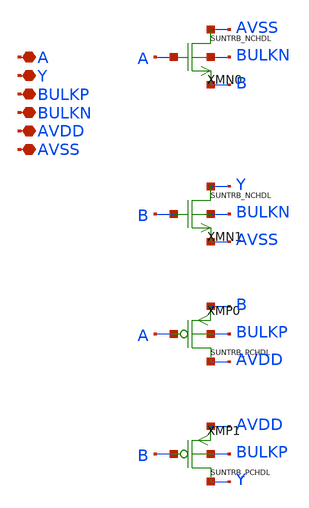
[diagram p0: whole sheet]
** sch_path: design/SUN_TRB_SKY130NM/SUNTRB_BFX1_CV.sch
**.subckt SUNTRB_BFX1_CV A Y BULKP BULKN AVDD AVSS
*.iopin A
*.iopin Y
*.iopin BULKP
*.iopin BULKN
*.iopin AVDD
*.iopin AVSS
XMN0 AVSS A B BULKN SUNTRB_NCHDL xoffset=0 yoffset=0 angle=0
XMN1 Y B AVSS BULKN SUNTRB_NCHDL xoffset=0 yoffset=0 angle=0
XMP0 AVDD A B BULKP SUNTRB_PCHDL xoffset=0 yoffset=0 angle=0 M=1
XMP1 Y B AVDD BULKP SUNTRB_PCHDL xoffset=0 yoffset=0 angle=0 M=1
**.ends
.end
